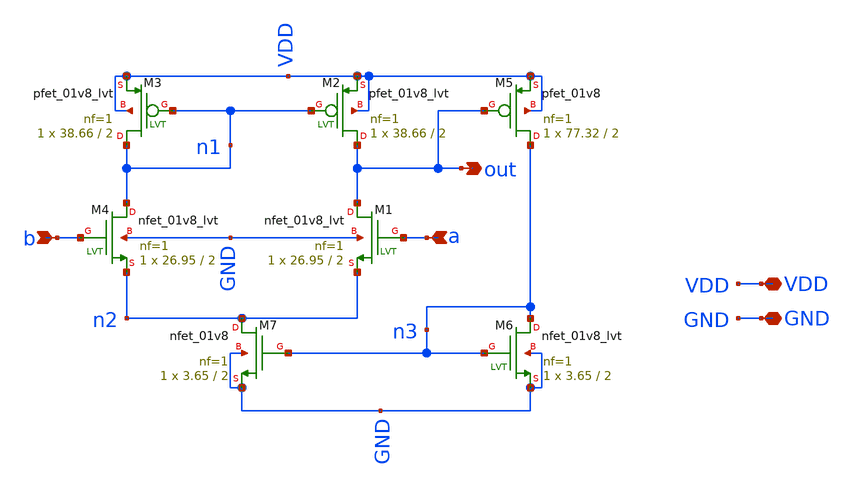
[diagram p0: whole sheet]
** sch_path: schematic/amp/amplifier_self_bias.sch
**.subckt amplifier_self_bias b a VDD out GND
*.ipin b
*.ipin a
*.iopin VDD
*.opin out
*.iopin GND
XM1 out a n2 GND sky130_fd_pr__nfet_01v8_lvt L=2 W=26.95 nf=1 ad='int((nf+1)/2) * W/nf * 0.29' as='int((nf+2)/2) * W/nf * 0.29'
+ pd='2*int((nf+1)/2) * (W/nf + 0.29)' ps='2*int((nf+2)/2) * (W/nf + 0.29)' nrd='0.29 / W' nrs='0.29 / W'
+ sa=0 sb=0 sd=0 mult=1 m=1
XM2 out n1 VDD VDD sky130_fd_pr__pfet_01v8_lvt L=2 W=38.66 nf=1 ad='int((nf+1)/2) * W/nf * 0.29' as='int((nf+2)/2) * W/nf * 0.29'
+ pd='2*int((nf+1)/2) * (W/nf + 0.29)' ps='2*int((nf+2)/2) * (W/nf + 0.29)' nrd='0.29 / W' nrs='0.29 / W'
+ sa=0 sb=0 sd=0 mult=1 m=1
XM3 n1 n1 VDD VDD sky130_fd_pr__pfet_01v8_lvt L=2 W=38.66 nf=1 ad='int((nf+1)/2) * W/nf * 0.29' as='int((nf+2)/2) * W/nf * 0.29'
+ pd='2*int((nf+1)/2) * (W/nf + 0.29)' ps='2*int((nf+2)/2) * (W/nf + 0.29)' nrd='0.29 / W' nrs='0.29 / W'
+ sa=0 sb=0 sd=0 mult=1 m=1
XM4 n1 b n2 GND sky130_fd_pr__nfet_01v8_lvt L=2 W=26.95 nf=1 ad='int((nf+1)/2) * W/nf * 0.29' as='int((nf+2)/2) * W/nf * 0.29'
+ pd='2*int((nf+1)/2) * (W/nf + 0.29)' ps='2*int((nf+2)/2) * (W/nf + 0.29)' nrd='0.29 / W' nrs='0.29 / W'
+ sa=0 sb=0 sd=0 mult=1 m=1
XM5 n3 out VDD VDD sky130_fd_pr__pfet_01v8 L=2 W=77.32 nf=1 ad='int((nf+1)/2) * W/nf * 0.29' as='int((nf+2)/2) * W/nf * 0.29'
+ pd='2*int((nf+1)/2) * (W/nf + 0.29)' ps='2*int((nf+2)/2) * (W/nf + 0.29)' nrd='0.29 / W' nrs='0.29 / W'
+ sa=0 sb=0 sd=0 mult=1 m=1
XM6 n3 n3 GND GND sky130_fd_pr__nfet_01v8_lvt L=2 W=3.65 nf=1 ad='int((nf+1)/2) * W/nf * 0.29' as='int((nf+2)/2) * W/nf * 0.29'
+ pd='2*int((nf+1)/2) * (W/nf + 0.29)' ps='2*int((nf+2)/2) * (W/nf + 0.29)' nrd='0.29 / W' nrs='0.29 / W'
+ sa=0 sb=0 sd=0 mult=1 m=1
XM7 n2 n3 GND GND sky130_fd_pr__nfet_01v8 L=2 W=3.65 nf=1 ad='int((nf+1)/2) * W/nf * 0.29' as='int((nf+2)/2) * W/nf * 0.29'
+ pd='2*int((nf+1)/2) * (W/nf + 0.29)' ps='2*int((nf+2)/2) * (W/nf + 0.29)' nrd='0.29 / W' nrs='0.29 / W'
+ sa=0 sb=0 sd=0 mult=1 m=1
**.ends
.end
